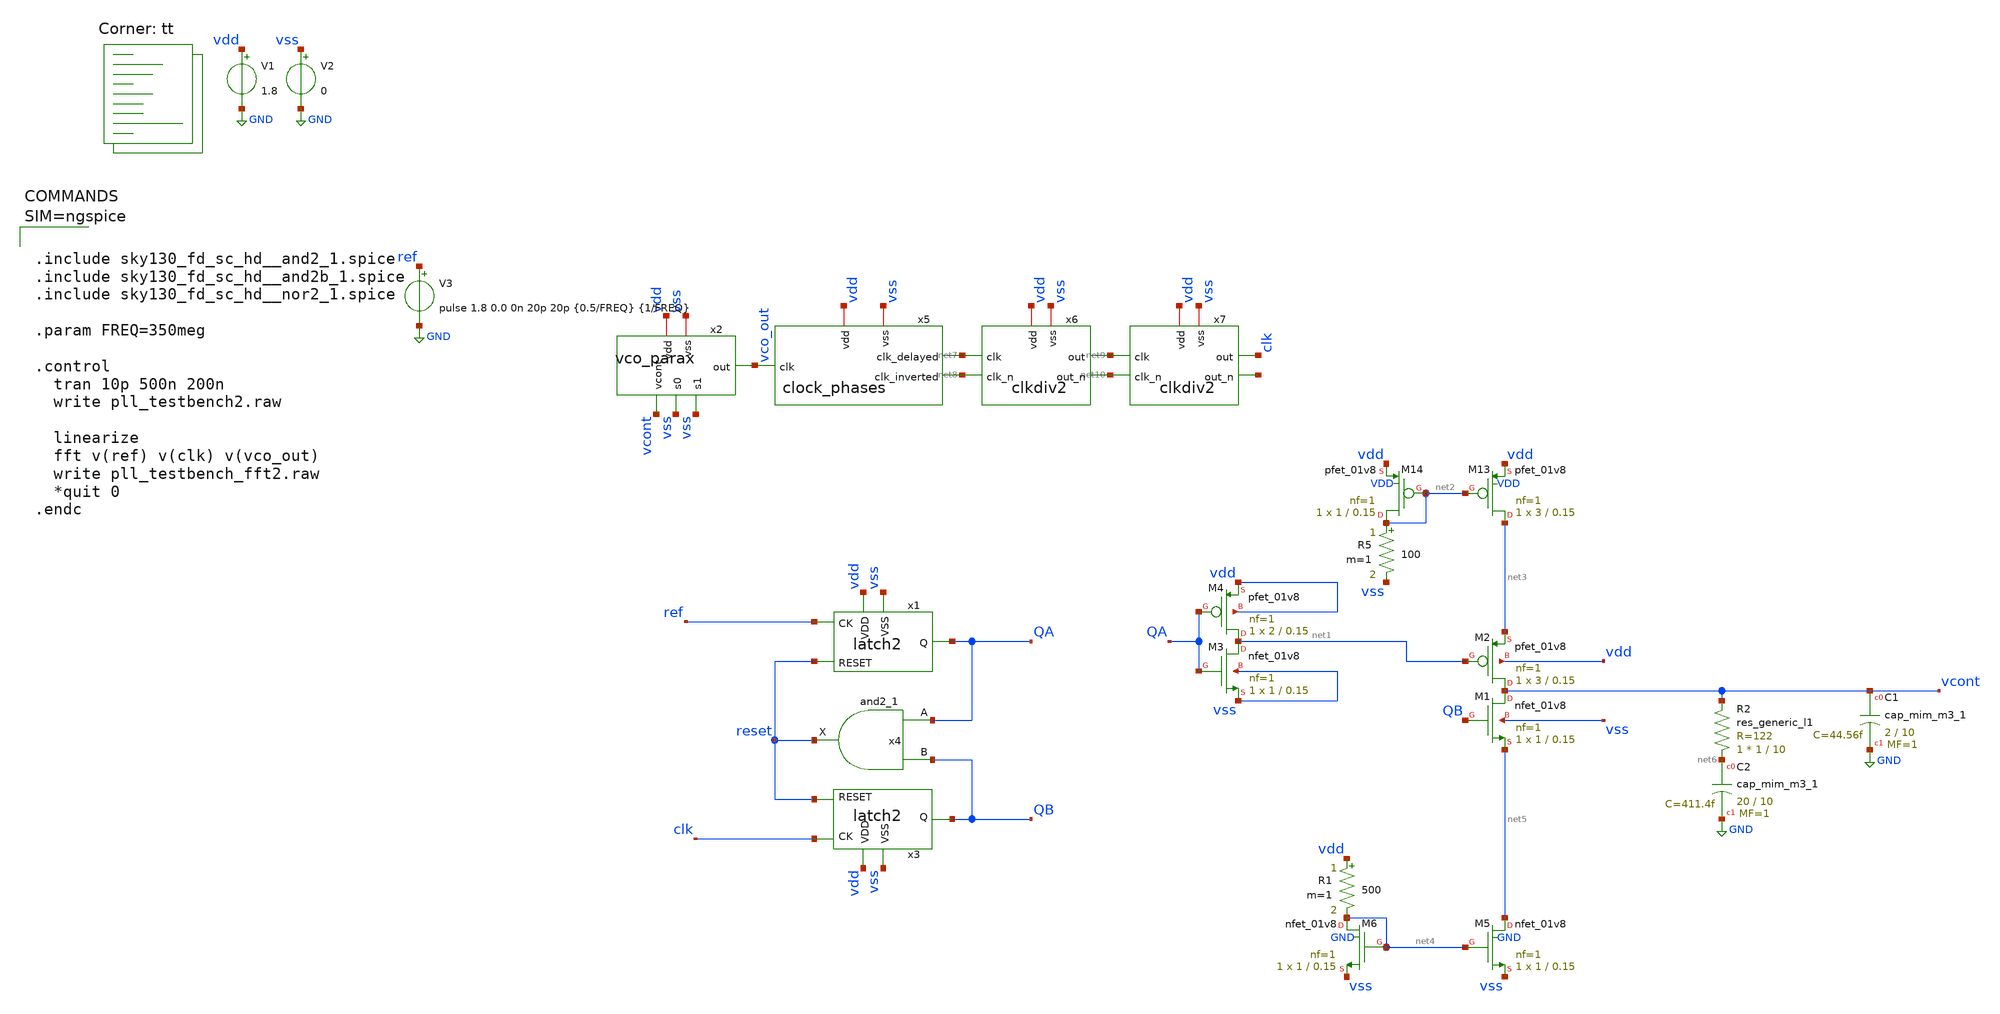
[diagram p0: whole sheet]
** sch_path: xschem/pll_testbench2.sch
**.subckt pll_testbench2
V1 vdd GND 1.8
V2 vss GND 0
x2 vdd vcont vss vss vco_out vss vco_parax
V3 ref GND pulse 1.8 0.0 0n 20p 20p {0.5/FREQ} {1/FREQ}
x1 ref QA reset vdd vss latch2
x3 clk QB reset vdd vss latch2
x4 QA QB vss vss vdd vdd reset sky130_fd_sc_hd__and2_1
XM1 vcont QB net5 vss sky130_fd_pr__nfet_01v8 L=0.15 W=1 nf=1 ad='int((nf+1)/2) * W/nf * 0.29' as='int((nf+2)/2) * W/nf * 0.29'
+ pd='2*int((nf+1)/2) * (W/nf + 0.29)' ps='2*int((nf+2)/2) * (W/nf + 0.29)' nrd='0.29 / W' nrs='0.29 / W'
+ sa=0 sb=0 sd=0 mult=1 m=1
XM2 vcont net1 net3 vdd sky130_fd_pr__pfet_01v8 L=0.15 W=3 nf=1 ad='int((nf+1)/2) * W/nf * 0.29' as='int((nf+2)/2) * W/nf * 0.29'
+ pd='2*int((nf+1)/2) * (W/nf + 0.29)' ps='2*int((nf+2)/2) * (W/nf + 0.29)' nrd='0.29 / W' nrs='0.29 / W'
+ sa=0 sb=0 sd=0 mult=1 m=1
XM3 net1 QA vss vss sky130_fd_pr__nfet_01v8 L=0.15 W=1 nf=1 ad='int((nf+1)/2) * W/nf * 0.29' as='int((nf+2)/2) * W/nf * 0.29'
+ pd='2*int((nf+1)/2) * (W/nf + 0.29)' ps='2*int((nf+2)/2) * (W/nf + 0.29)' nrd='0.29 / W' nrs='0.29 / W'
+ sa=0 sb=0 sd=0 mult=1 m=1
XM4 net1 QA vdd vdd sky130_fd_pr__pfet_01v8 L=0.15 W=2 nf=1 ad='int((nf+1)/2) * W/nf * 0.29' as='int((nf+2)/2) * W/nf * 0.29'
+ pd='2*int((nf+1)/2) * (W/nf + 0.29)' ps='2*int((nf+2)/2) * (W/nf + 0.29)' nrd='0.29 / W' nrs='0.29 / W'
+ sa=0 sb=0 sd=0 mult=1 m=1
XC2 net6 GND sky130_fd_pr__cap_mim_m3_1 W=20 L=10 MF=1 m=1
R2 net6 vcont sky130_fd_pr__res_generic_l1 W=1 L=10 m=1
XC1 vcont GND sky130_fd_pr__cap_mim_m3_1 W=2 L=10 MF=1 m=1
XM13 net3 net2 vdd VDD sky130_fd_pr__pfet_01v8 L=0.15 W=3 nf=1 ad='int((nf+1)/2) * W/nf * 0.29' as='int((nf+2)/2) * W/nf * 0.29'
+ pd='2*int((nf+1)/2) * (W/nf + 0.29)' ps='2*int((nf+2)/2) * (W/nf + 0.29)' nrd='0.29 / W' nrs='0.29 / W'
+ sa=0 sb=0 sd=0 mult=1 m=1
XM14 net2 net2 vdd VDD sky130_fd_pr__pfet_01v8 L=0.15 W=1 nf=1 ad='int((nf+1)/2) * W/nf * 0.29' as='int((nf+2)/2) * W/nf * 0.29'
+ pd='2*int((nf+1)/2) * (W/nf + 0.29)' ps='2*int((nf+2)/2) * (W/nf + 0.29)' nrd='0.29 / W' nrs='0.29 / W'
+ sa=0 sb=0 sd=0 mult=1 m=1
R5 net2 vss 100 m=1
R1 vdd net4 500 m=1
XM5 net5 net4 vss GND sky130_fd_pr__nfet_01v8 L=0.15 W=1 nf=1 ad='int((nf+1)/2) * W/nf * 0.29' as='int((nf+2)/2) * W/nf * 0.29'
+ pd='2*int((nf+1)/2) * (W/nf + 0.29)' ps='2*int((nf+2)/2) * (W/nf + 0.29)' nrd='0.29 / W' nrs='0.29 / W'
+ sa=0 sb=0 sd=0 mult=1 m=1
XM6 net4 net4 vss GND sky130_fd_pr__nfet_01v8 L=0.15 W=1 nf=1 ad='int((nf+1)/2) * W/nf * 0.29' as='int((nf+2)/2) * W/nf * 0.29'
+ pd='2*int((nf+1)/2) * (W/nf + 0.29)' ps='2*int((nf+2)/2) * (W/nf + 0.29)' nrd='0.29 / W' nrs='0.29 / W'
+ sa=0 sb=0 sd=0 mult=1 m=1
x5 vdd net7 vco_out net8 vss clock_phases
x6 vdd vss net9 net10 net8 net7 clkdiv2
x7 vdd vss clk net11 net10 net9 clkdiv2
**** begin user architecture code
.lib $::SKYWATER_MODELS/sky130.lib.spice tt



.include sky130_fd_sc_hd__and2_1.spice
.include sky130_fd_sc_hd__and2b_1.spice
.include sky130_fd_sc_hd__nor2_1.spice

.param FREQ=350meg

.control
  tran 10p 500n 200n
  write pll_testbench2.raw

  linearize
  fft v(ref) v(clk) v(vco_out)
  write pll_testbench_fft2.raw
  *quit 0
.endc



**** end user architecture code
**.ends

* expanding   symbol:  vco_parax.sym # of pins=6
** sym_path: xschem/vco.sym
.include [file normalize ../mag/vco.sim.spice]

* expanding   symbol:  latch2.sym # of pins=5
** sym_path: xschem/latch2.sym
** sch_path: xschem/latch2.sch
.subckt latch2 CK Q RESET VDD VSS
*.ipin RESET
*.ipin CK
*.opin Q
*.ipin VDD
*.ipin VSS
x1 net3 net2 VSS VSS VDD VDD net1 sky130_fd_sc_hd__nor2_1
x2 net1 RESET VSS VSS VDD VDD net2 sky130_fd_sc_hd__nor2_1
x3 CK Q VSS VSS VDD VDD net3 sky130_fd_sc_hd__nor2_1
x4 net3 net1 VSS VSS VDD VDD Q sky130_fd_sc_hd__nor2_1
.ends


* expanding   symbol:  clock_phases.sym # of pins=5
** sym_path: xschem/clock_phases.sym
** sch_path: xschem/clock_phases.sch
.subckt clock_phases vdd clk_delayed clk clk_inverted vss
*.ipin clk
*.iopin vdd
*.opin clk_delayed
*.opin clk_inverted
*.iopin vss
XM3 net2 clk vss GND sky130_fd_pr__nfet_01v8 L=0.15 W=1 nf=1 ad='int((nf+1)/2) * W/nf * 0.29' as='int((nf+2)/2) * W/nf * 0.29'
+ pd='2*int((nf+1)/2) * (W/nf + 0.29)' ps='2*int((nf+2)/2) * (W/nf + 0.29)' nrd='0.29 / W' nrs='0.29 / W'
+ sa=0 sb=0 sd=0 mult=1 m=1
XM4 net2 clk vdd VDD sky130_fd_pr__pfet_01v8 L=0.15 W=1 nf=2 ad='int((nf+1)/2) * W/nf * 0.29' as='int((nf+2)/2) * W/nf * 0.29'
+ pd='2*int((nf+1)/2) * (W/nf + 0.29)' ps='2*int((nf+2)/2) * (W/nf + 0.29)' nrd='0.29 / W' nrs='0.29 / W'
+ sa=0 sb=0 sd=0 mult=1 m=1
XM5 net1 vdd clk GND sky130_fd_pr__nfet_01v8 L=0.15 W=1 nf=1 ad='int((nf+1)/2) * W/nf * 0.29' as='int((nf+2)/2) * W/nf * 0.29'
+ pd='2*int((nf+1)/2) * (W/nf + 0.29)' ps='2*int((nf+2)/2) * (W/nf + 0.29)' nrd='0.29 / W' nrs='0.29 / W'
+ sa=0 sb=0 sd=0 mult=1 m=1
XM6 net1 vss clk VDD sky130_fd_pr__pfet_01v8 L=0.15 W=1 nf=2 ad='int((nf+1)/2) * W/nf * 0.29' as='int((nf+2)/2) * W/nf * 0.29'
+ pd='2*int((nf+1)/2) * (W/nf + 0.29)' ps='2*int((nf+2)/2) * (W/nf + 0.29)' nrd='0.29 / W' nrs='0.29 / W'
+ sa=0 sb=0 sd=0 mult=1 m=1
XM7 clk_delayed net2 vss GND sky130_fd_pr__nfet_01v8 L=0.15 W=1 nf=1 ad='int((nf+1)/2) * W/nf * 0.29'
+ as='int((nf+2)/2) * W/nf * 0.29' pd='2*int((nf+1)/2) * (W/nf + 0.29)' ps='2*int((nf+2)/2) * (W/nf + 0.29)'
+ nrd='0.29 / W' nrs='0.29 / W' sa=0 sb=0 sd=0 mult=1 m=1
XM8 clk_delayed net2 vdd VDD sky130_fd_pr__pfet_01v8 L=0.15 W=1 nf=2 ad='int((nf+1)/2) * W/nf * 0.29'
+ as='int((nf+2)/2) * W/nf * 0.29' pd='2*int((nf+1)/2) * (W/nf + 0.29)' ps='2*int((nf+2)/2) * (W/nf + 0.29)'
+ nrd='0.29 / W' nrs='0.29 / W' sa=0 sb=0 sd=0 mult=1 m=1
XM9 clk_inverted net1 vss GND sky130_fd_pr__nfet_01v8 L=0.15 W=1 nf=1 ad='int((nf+1)/2) * W/nf * 0.29'
+ as='int((nf+2)/2) * W/nf * 0.29' pd='2*int((nf+1)/2) * (W/nf + 0.29)' ps='2*int((nf+2)/2) * (W/nf + 0.29)'
+ nrd='0.29 / W' nrs='0.29 / W' sa=0 sb=0 sd=0 mult=1 m=1
XM10 clk_inverted net1 vdd VDD sky130_fd_pr__pfet_01v8 L=0.15 W=1 nf=2 ad='int((nf+1)/2) * W/nf * 0.29'
+ as='int((nf+2)/2) * W/nf * 0.29' pd='2*int((nf+1)/2) * (W/nf + 0.29)' ps='2*int((nf+2)/2) * (W/nf + 0.29)'
+ nrd='0.29 / W' nrs='0.29 / W' sa=0 sb=0 sd=0 mult=1 m=1
.ends


* expanding   symbol:  clkdiv2.sym # of pins=6
** sym_path: xschem/clkdiv2.sym
** sch_path: xschem/clkdiv2.sch
.subckt clkdiv2 vdd vss out out_n clk_n clk
*.iopin vdd
*.opin out
*.iopin vss
*.ipin clk
*.opin out_n
*.ipin clk_n
x2 vdd vss net1 net2 out_n out clk latch
x3 vdd vss out_n out net2 net1 clk_n latch
.ends


* expanding   symbol:  latch.sym # of pins=7
** sym_path: xschem/latch.sym
** sch_path: xschem/latch.sch
.subckt latch vdd vss q_n q d d_n clk
*.iopin vdd
*.ipin d
*.opin q
*.iopin vss
*.ipin d_n
*.opin q_n
*.ipin clk
XM11 q_n q vdd vdd sky130_fd_pr__pfet_01v8 L=0.15 W=2 nf=1 ad='int((nf+1)/2) * W/nf * 0.29' as='int((nf+2)/2) * W/nf * 0.29'
+ pd='2*int((nf+1)/2) * (W/nf + 0.29)' ps='2*int((nf+2)/2) * (W/nf + 0.29)' nrd='0.29 / W' nrs='0.29 / W'
+ sa=0 sb=0 sd=0 mult=1 m=1
XM12 q q_n vdd vdd sky130_fd_pr__pfet_01v8 L=0.15 W=2 nf=1 ad='int((nf+1)/2) * W/nf * 0.29' as='int((nf+2)/2) * W/nf * 0.29'
+ pd='2*int((nf+1)/2) * (W/nf + 0.29)' ps='2*int((nf+2)/2) * (W/nf + 0.29)' nrd='0.29 / W' nrs='0.29 / W'
+ sa=0 sb=0 sd=0 mult=1 m=1
XM13 q_n d net1 vss sky130_fd_pr__nfet_01v8 L=0.15 W=1 nf=1 ad='int((nf+1)/2) * W/nf * 0.29' as='int((nf+2)/2) * W/nf * 0.29'
+ pd='2*int((nf+1)/2) * (W/nf + 0.29)' ps='2*int((nf+2)/2) * (W/nf + 0.29)' nrd='0.29 / W' nrs='0.29 / W'
+ sa=0 sb=0 sd=0 mult=1 m=1
XM14 q d_n net1 vss sky130_fd_pr__nfet_01v8 L=0.15 W=1 nf=1 ad='int((nf+1)/2) * W/nf * 0.29' as='int((nf+2)/2) * W/nf * 0.29'
+ pd='2*int((nf+1)/2) * (W/nf + 0.29)' ps='2*int((nf+2)/2) * (W/nf + 0.29)' nrd='0.29 / W' nrs='0.29 / W'
+ sa=0 sb=0 sd=0 mult=1 m=1
XM15 net1 clk vss vss sky130_fd_pr__nfet_01v8 L=0.15 W=2 nf=1 ad='int((nf+1)/2) * W/nf * 0.29' as='int((nf+2)/2) * W/nf * 0.29'
+ pd='2*int((nf+1)/2) * (W/nf + 0.29)' ps='2*int((nf+2)/2) * (W/nf + 0.29)' nrd='0.29 / W' nrs='0.29 / W'
+ sa=0 sb=0 sd=0 mult=1 m=1
.ends

.GLOBAL GND
.end
